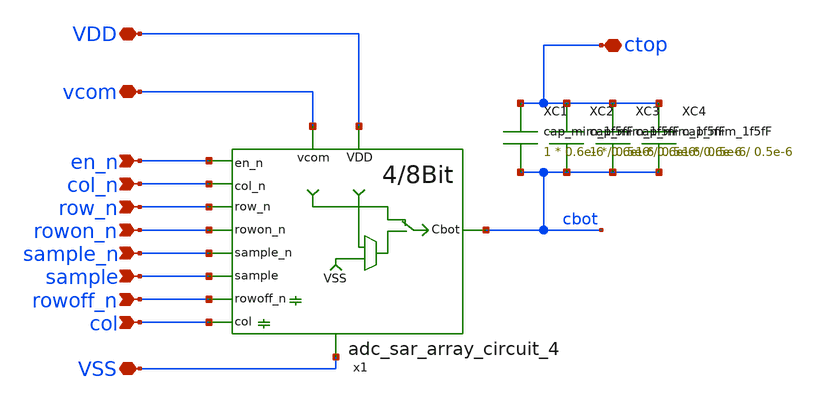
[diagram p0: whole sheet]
** sch_path: adc_sar_wafflecap_8_4.sch
**.subckt adc_sar_wafflecap_8_4 vcom VDD ctop VSS en_n row_n col_n rowon_n sample_n sample rowoff_n
*+ col
*.iopin vcom
*.iopin VDD
*.iopin ctop
*.iopin VSS
*.ipin en_n
*.ipin row_n
*.ipin col_n
*.ipin rowon_n
*.ipin sample_n
*.ipin sample
*.ipin rowoff_n
*.ipin col
x1 VDD col_n cbot row_n rowon_n sample_n vcom sample VSS en_n rowoff_n col adc_sar_array_circuit_4
XC1 ctop cbot cap_mim_1f5fF c_width=0.6e-6 c_length=0.5e-6 m=1
XC2 ctop cbot cap_mim_1f5fF c_width=0.6e-6 c_length=0.5e-6 m=1
XC3 ctop cbot cap_mim_1f5fF c_width=0.6e-6 c_length=0.5e-6 m=1
XC4 ctop cbot cap_mim_1f5fF c_width=0.6e-6 c_length=0.5e-6 m=1
**.ends

* expanding   symbol:  adc_sar_array_circuit_4.sym # of pins=12
** sym_path: adc_sar_array_circuit_4.sym
** sch_path: adc_sar_array_circuit_4.sch
.subckt adc_sar_array_circuit_4 VDD col_n Cbot row_n rowon_n sample_n vcom sample VSS en_n rowoff_n
+ col
*.ipin sample_n
*.ipin sample
*.iopin vcom
*.ipin row_n
*.ipin col_n
*.ipin rowon_n
*.iopin VDD
*.iopin VSS
*.iopin Cbot
*.ipin en_n
*.ipin rowoff_n
*.ipin col
* noconn row_n
* noconn col_n
* noconn rowon_n
* noconn rowoff_n
* noconn col
XM1 vcom sample_n Cbot VDD pfet_03v3 L=0.28u W=0.8u nf=1 ad='int((nf+1)/2) * W/nf * 0.18u' as='int((nf+2)/2) * W/nf * 0.18u'
+ pd='2*int((nf+1)/2) * (W/nf + 0.18u)' ps='2*int((nf+2)/2) * (W/nf + 0.18u)' nrd='0.18u / W' nrs='0.18u / W'
+ sa=0 sb=0 sd=0 m=1
XM2 vdrv sample_n Cbot VSS nfet_03v3 L=0.28u W=0.42u nf=1 ad='int((nf+1)/2) * W/nf * 0.18u' as='int((nf+2)/2) * W/nf * 0.18u'
+ pd='2*int((nf+1)/2) * (W/nf + 0.18u)' ps='2*int((nf+2)/2) * (W/nf + 0.18u)' nrd='0.18u / W' nrs='0.18u / W'
+ sa=0 sb=0 sd=0 m=1
XM3 vdrv sample Cbot VDD pfet_03v3 L=0.28u W=0.8u nf=1 ad='int((nf+1)/2) * W/nf * 0.18u' as='int((nf+2)/2) * W/nf * 0.18u'
+ pd='2*int((nf+1)/2) * (W/nf + 0.18u)' ps='2*int((nf+2)/2) * (W/nf + 0.18u)' nrd='0.18u / W' nrs='0.18u / W'
+ sa=0 sb=0 sd=0 m=1
XM4 vcom sample Cbot VSS nfet_03v3 L=0.28u W=0.42u nf=1 ad='int((nf+1)/2) * W/nf * 0.18u' as='int((nf+2)/2) * W/nf * 0.18u'
+ pd='2*int((nf+1)/2) * (W/nf + 0.18u)' ps='2*int((nf+2)/2) * (W/nf + 0.18u)' nrd='0.18u / W' nrs='0.18u / W'
+ sa=0 sb=0 sd=0 m=1
XM5 VDD en_n vint1 VDD pfet_03v3 L=0.28u W=0.8u nf=1 ad='int((nf+1)/2) * W/nf * 0.18u' as='int((nf+2)/2) * W/nf * 0.18u'
+ pd='2*int((nf+1)/2) * (W/nf + 0.18u)' ps='2*int((nf+2)/2) * (W/nf + 0.18u)' nrd='0.18u / W' nrs='0.18u / W'
+ sa=0 sb=0 sd=0 m=1
XM6 vint1 en_n vdrv VDD pfet_03v3 L=0.28u W=0.8u nf=1 ad='int((nf+1)/2) * W/nf * 0.18u' as='int((nf+2)/2) * W/nf * 0.18u'
+ pd='2*int((nf+1)/2) * (W/nf + 0.18u)' ps='2*int((nf+2)/2) * (W/nf + 0.18u)' nrd='0.18u / W' nrs='0.18u / W'
+ sa=0 sb=0 sd=0 m=1
XM7 VDD en_n vdrv VDD pfet_03v3 L=0.28u W=0.8u nf=1 ad='int((nf+1)/2) * W/nf * 0.18u' as='int((nf+2)/2) * W/nf * 0.18u'
+ pd='2*int((nf+1)/2) * (W/nf + 0.18u)' ps='2*int((nf+2)/2) * (W/nf + 0.18u)' nrd='0.18u / W' nrs='0.18u / W'
+ sa=0 sb=0 sd=0 m=1
XM8 vint2 en_n vdrv VSS nfet_03v3 L=0.28u W=0.42u nf=1 ad='int((nf+1)/2) * W/nf * 0.18u' as='int((nf+2)/2) * W/nf * 0.18u'
+ pd='2*int((nf+1)/2) * (W/nf + 0.18u)' ps='2*int((nf+2)/2) * (W/nf + 0.18u)' nrd='0.18u / W' nrs='0.18u / W'
+ sa=0 sb=0 sd=0 m=1
XM9 VSS en_n vint2 VSS nfet_03v3 L=0.28u W=0.42u nf=1 ad='int((nf+1)/2) * W/nf * 0.18u' as='int((nf+2)/2) * W/nf * 0.18u'
+ pd='2*int((nf+1)/2) * (W/nf + 0.18u)' ps='2*int((nf+2)/2) * (W/nf + 0.18u)' nrd='0.18u / W' nrs='0.18u / W'
+ sa=0 sb=0 sd=0 m=1
XM10 VSS en_n vint2 VSS nfet_03v3 L=0.28u W=0.42u nf=1 ad='int((nf+1)/2) * W/nf * 0.18u' as='int((nf+2)/2) * W/nf * 0.18u'
+ pd='2*int((nf+1)/2) * (W/nf + 0.18u)' ps='2*int((nf+2)/2) * (W/nf + 0.18u)' nrd='0.18u / W' nrs='0.18u / W'
+ sa=0 sb=0 sd=0 m=1
.ends

.end
